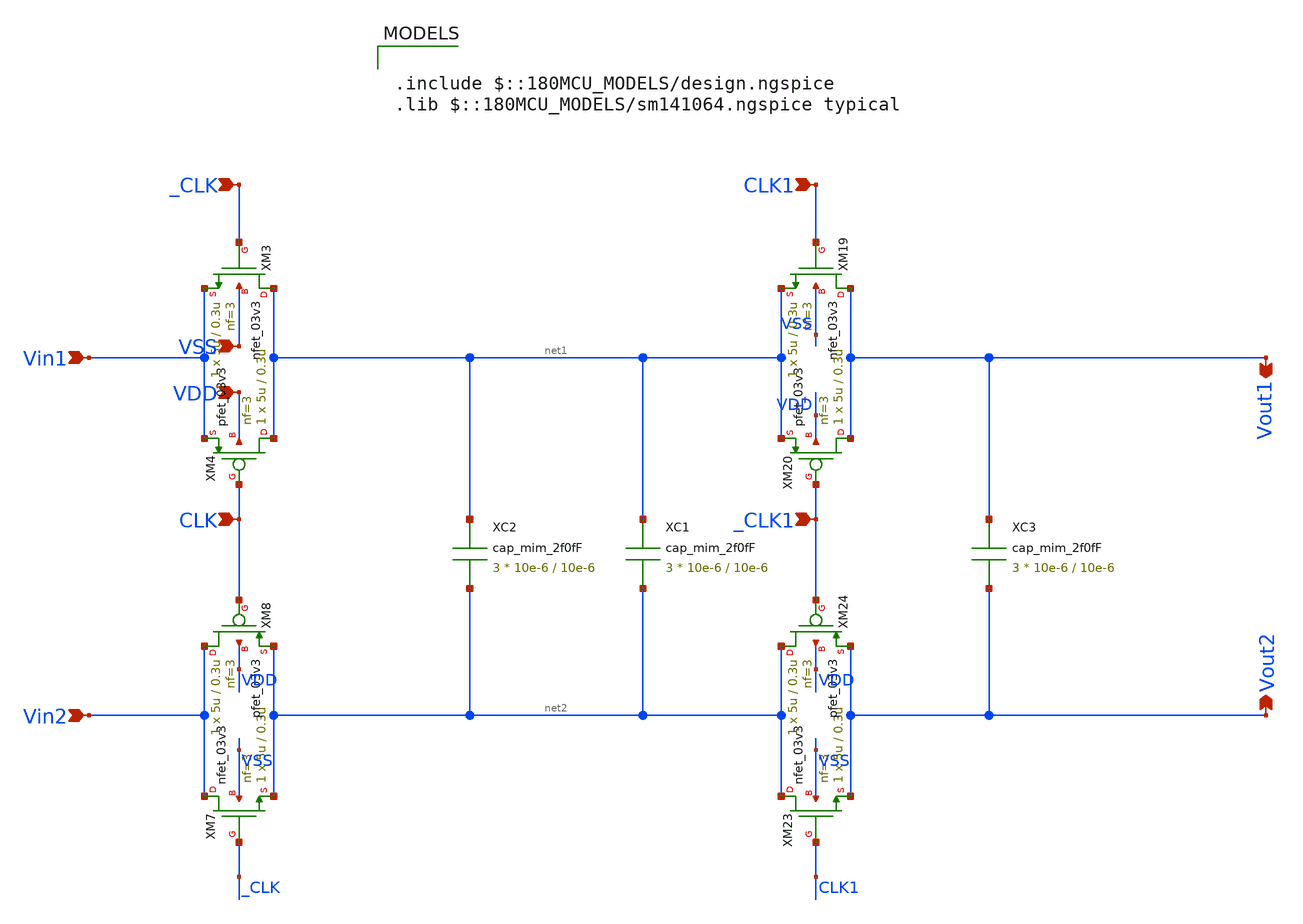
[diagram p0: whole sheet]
** sch_path: FULL_SCH_FILE/LPF/lpf.sch
**.subckt lpf VSS VDD _CLK CLK Vin1 Vin2 CLK1 _CLK1 Vout1 Vout2
*.ipin VSS
*.ipin VDD
*.ipin _CLK
*.ipin CLK
*.ipin Vin1
*.ipin Vin2
*.ipin CLK1
*.ipin _CLK1
*.opin Vout1
*.opin Vout2
XM3 net1 _CLK Vin1 VSS nfet_03v3 L=0.3u W=5u nf=3 ad='int((nf+1)/2) * W/nf * 0.18u' as='int((nf+2)/2) * W/nf * 0.18u'
+ pd='2*int((nf+1)/2) * (W/nf + 0.18u)' ps='2*int((nf+2)/2) * (W/nf + 0.18u)' nrd='0.18u / W' nrs='0.18u / W'
+ sa=0 sb=0 sd=0 m=1
XM4 net1 CLK Vin1 VDD pfet_03v3 L=0.3u W=5u nf=3 ad='int((nf+1)/2) * W/nf * 0.18u' as='int((nf+2)/2) * W/nf * 0.18u'
+ pd='2*int((nf+1)/2) * (W/nf + 0.18u)' ps='2*int((nf+2)/2) * (W/nf + 0.18u)' nrd='0.18u / W' nrs='0.18u / W'
+ sa=0 sb=0 sd=0 m=1
XM7 Vin2 _CLK net2 VSS nfet_03v3 L=0.3u W=5u nf=3 ad='int((nf+1)/2) * W/nf * 0.18u' as='int((nf+2)/2) * W/nf * 0.18u'
+ pd='2*int((nf+1)/2) * (W/nf + 0.18u)' ps='2*int((nf+2)/2) * (W/nf + 0.18u)' nrd='0.18u / W' nrs='0.18u / W'
+ sa=0 sb=0 sd=0 m=1
XM8 Vin2 CLK net2 VDD pfet_03v3 L=0.3u W=5u nf=3 ad='int((nf+1)/2) * W/nf * 0.18u' as='int((nf+2)/2) * W/nf * 0.18u'
+ pd='2*int((nf+1)/2) * (W/nf + 0.18u)' ps='2*int((nf+2)/2) * (W/nf + 0.18u)' nrd='0.18u / W' nrs='0.18u / W'
+ sa=0 sb=0 sd=0 m=1
XM19 Vout1 CLK1 net1 VSS nfet_03v3 L=0.3u W=5u nf=3 ad='int((nf+1)/2) * W/nf * 0.18u' as='int((nf+2)/2) * W/nf * 0.18u'
+ pd='2*int((nf+1)/2) * (W/nf + 0.18u)' ps='2*int((nf+2)/2) * (W/nf + 0.18u)' nrd='0.18u / W' nrs='0.18u / W'
+ sa=0 sb=0 sd=0 m=1
XM20 Vout1 _CLK1 net1 VDD pfet_03v3 L=0.3u W=5u nf=3 ad='int((nf+1)/2) * W/nf * 0.18u' as='int((nf+2)/2) * W/nf * 0.18u'
+ pd='2*int((nf+1)/2) * (W/nf + 0.18u)' ps='2*int((nf+2)/2) * (W/nf + 0.18u)' nrd='0.18u / W' nrs='0.18u / W'
+ sa=0 sb=0 sd=0 m=1
XM23 net2 CLK1 Vout2 VSS nfet_03v3 L=0.3u W=5u nf=3 ad='int((nf+1)/2) * W/nf * 0.18u' as='int((nf+2)/2) * W/nf * 0.18u'
+ pd='2*int((nf+1)/2) * (W/nf + 0.18u)' ps='2*int((nf+2)/2) * (W/nf + 0.18u)' nrd='0.18u / W' nrs='0.18u / W'
+ sa=0 sb=0 sd=0 m=1
XM24 net2 _CLK1 Vout2 VDD pfet_03v3 L=0.3u W=5u nf=3 ad='int((nf+1)/2) * W/nf * 0.18u' as='int((nf+2)/2) * W/nf * 0.18u'
+ pd='2*int((nf+1)/2) * (W/nf + 0.18u)' ps='2*int((nf+2)/2) * (W/nf + 0.18u)' nrd='0.18u / W' nrs='0.18u / W'
+ sa=0 sb=0 sd=0 m=1
XC1 net1 net2 cap_mim_2f0fF c_width=10e-6 c_length=10e-6 m=3
XC2 net1 net2 cap_mim_2f0fF c_width=10e-6 c_length=10e-6 m=3
XC3 Vout1 Vout2 cap_mim_2f0fF c_width=10e-6 c_length=10e-6 m=3
**** begin user architecture code

.include $::180MCU_MODELS/design.ngspice
.lib $::180MCU_MODELS/sm141064.ngspice typical

**** end user architecture code
**.ends
.end
